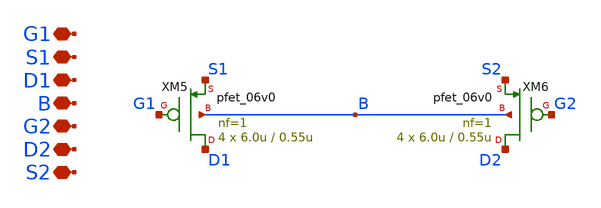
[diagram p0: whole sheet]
** sch_path: designs/libs/core_single-fet/pfet-pin/pfet-pin.sch
**.subckt pfet-pin S1 B G1 D1 S2 G2 D2
*.iopin S1
*.iopin B
*.iopin G1
*.iopin D1
*.iopin S2
*.iopin G2
*.iopin D2
XM5 D1 G1 S1 B pfet_06v0 L=0.55u W=6.0u nf=1 ad='int((nf+1)/2) * W/nf * 0.18u' as='int((nf+2)/2) * W/nf * 0.18u'
+ pd='2*int((nf+1)/2) * (W/nf + 0.18u)' ps='2*int((nf+2)/2) * (W/nf + 0.18u)' nrd='0.18u / W' nrs='0.18u / W'
+ sa=0 sb=0 sd=0 m=4
XM6 D2 G2 S2 B pfet_06v0 L=0.55u W=6.0u nf=1 ad='int((nf+1)/2) * W/nf * 0.18u' as='int((nf+2)/2) * W/nf * 0.18u'
+ pd='2*int((nf+1)/2) * (W/nf + 0.18u)' ps='2*int((nf+2)/2) * (W/nf + 0.18u)' nrd='0.18u / W' nrs='0.18u / W'
+ sa=0 sb=0 sd=0 m=4
**.ends
.end
